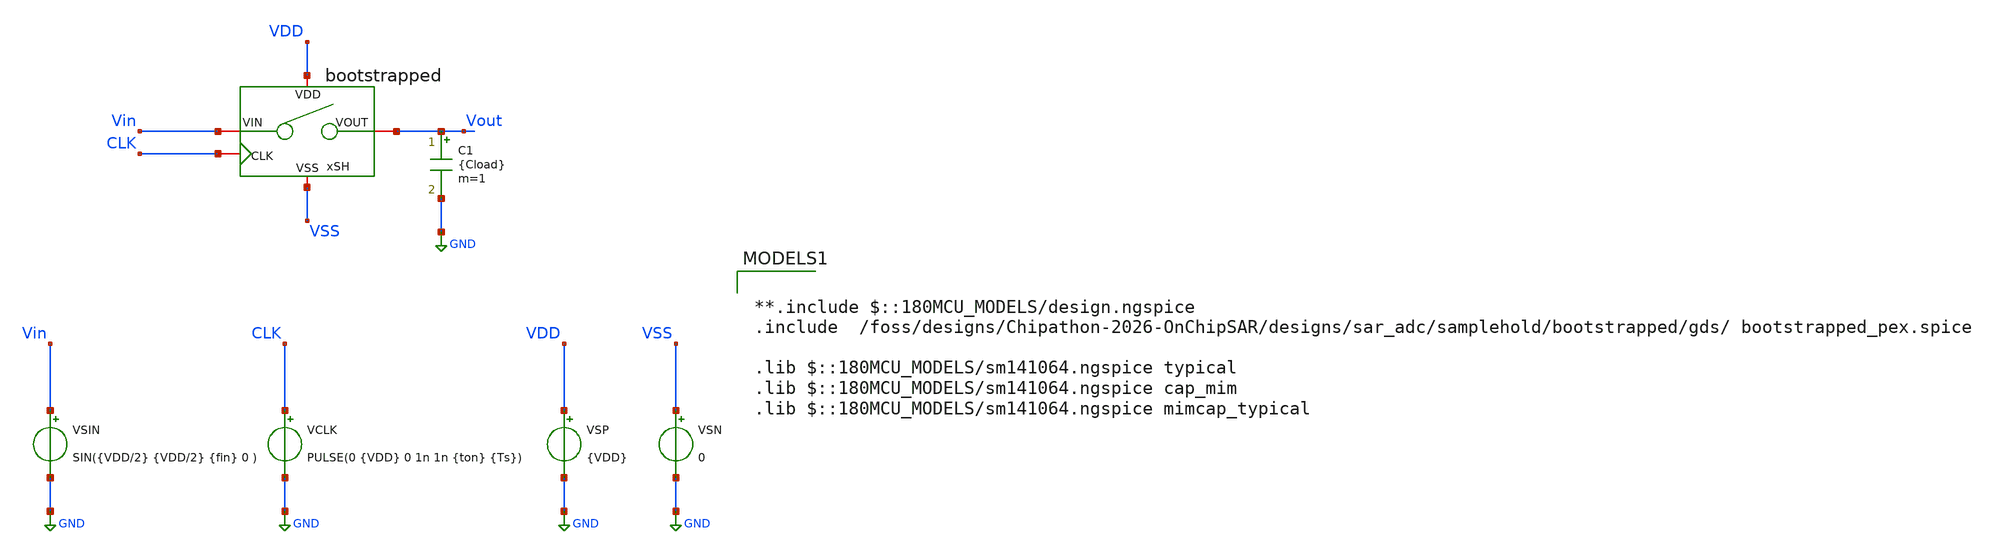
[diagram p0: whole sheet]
** sch_path: designs/sar_adc/samplehold/bootstrapped/xschem/tb_bootstrapped.sch
**.subckt tb_bootstrapped
VSP VDD GND {VDD}
VSN VSS GND 0
VSIN Vin GND SIN({VDD/2} {VDD/2} {fin} 0 )
VCLK CLK GND PULSE(0 {VDD} 0 1n 1n {ton} {Ts})
C1 Vout GND {Cload} m=1
xSH VDD VSS CLK Vin Vout bootstrapped
**** begin user architecture code

**.include $::180MCU_MODELS/design.ngspice
.include  /foss/designs/Chipathon-2026-OnChipSAR/designs/sar_adc/samplehold/bootstrapped/gds/ bootstrapped_pex.spice

.lib $::180MCU_MODELS/sm141064.ngspice typical
.lib $::180MCU_MODELS/sm141064.ngspice cap_mim
.lib $::180MCU_MODELS/sm141064.ngspice mimcap_typical





* Sampling clock
.param Fs = 5Meg
.param ton = Ts/12

* Input parameters
.param Ts = 1/Fs
.param Ns = 1024
.param Nc = 103
.param fin = Nc/Ns*Fs
.param sw_stat_mismatch=0
.param fnoicor=0

* Test-bench parameters
.temp 27
.param VDD = 3.3
.param Cload = 1p

.save all

.control

* Local variables for .control
let Fs = 5Meg
let Ns = 1024
let Nspare = 5

let tstep = 1/(Fs*250)
let tstop = (Ns + Nspare)/Fs

* Transient simulation
tran $&tstep $&tstop

* Power calculation
let P_DD=-v(vdd)*i(vsp)
meas tran P_avg AVG P_DD from=0 to=tstop
print P_avg

linearize v(vout) v(vin) v(clk) P_DD
wrdata tb_bootstrapped.csv v(vin) v(vout) v(clk) P_DD

plot v(vin) v(vout)
plot v(vin) v(vout) xl 0 4u

.endc



**** end user architecture code
**.ends
.GLOBAL GND
.end
